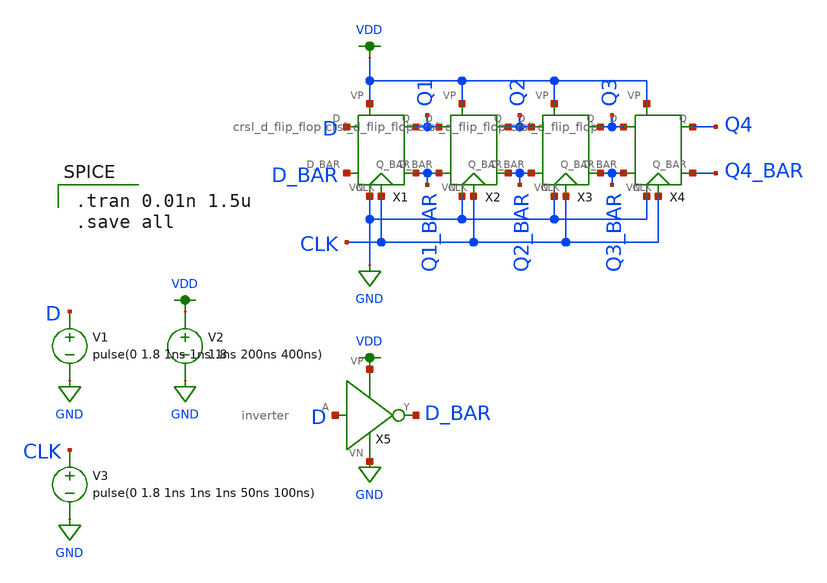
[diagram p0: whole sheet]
** sch_path: mp2/schematics/crsl_d_flip_flop_tran.sch
**.subckt crsl_d_flip_flop_tran
V1 D GND pulse(0 1.8 1ns 1ns 1ns 200ns 400ns)
X4 Q3 Q3_BAR Q4_BAR VDD Q4 CLK GND crsl_d_flip_flop
X5 D VDD GND D_BAR inverter
V2 VDD GND 1.8
V3 CLK GND pulse(0 1.8 1ns 1ns 1ns 50ns 100ns)
X1 D D_BAR Q1_BAR VDD Q1 CLK GND crsl_d_flip_flop
X2 Q1 Q1_BAR Q2_BAR VDD Q2 CLK GND crsl_d_flip_flop
X3 Q2 Q2_BAR Q3_BAR VDD Q3 CLK GND crsl_d_flip_flop
**** begin user architecture code

.option wnflag=1
.lib ~/skywater/skywater-pdk/libraries/sky130_fd_pr_ngspice/latest/models/sky130.lib.spice tt


.tran 0.01n 1.5u
.save all

**** end user architecture code
**.ends

* expanding   symbol:  /home/madvlsi/Documents/VLSI/mp2/schematics/crsl_d_flip_flop.sym # of pins=7
** sym_path: mp2/schematics/crsl_d_flip_flop.sym
** sch_path: mp2/schematics/crsl_d_flip_flop.sch
.subckt crsl_d_flip_flop D D_BAR Q_BAR VP Q CLK VN
*.ipin D
*.ipin D_BAR
*.iopin VP
*.iopin VN
*.opin Q
*.opin Q_BAR
*.ipin CLK
XM1 net1 CLK D VP sky130_fd_pr__pfet_01v8 L=0.15 W=1 nf=1 ad='int((nf+1)/2) * W/nf * 0.29' as='int((nf+2)/2) * W/nf * 0.29'
+ pd='2*int((nf+1)/2) * (W/nf + 0.29)' ps='2*int((nf+2)/2) * (W/nf + 0.29)' nrd='0.29 / W' nrs='0.29 / W'
+ sa=0 sb=0 sd=0 mult=1 m=1
XM2 net2 CLK D_BAR VP sky130_fd_pr__pfet_01v8 L=0.15 W=1 nf=1 ad='int((nf+1)/2) * W/nf * 0.29' as='int((nf+2)/2) * W/nf * 0.29'
+ pd='2*int((nf+1)/2) * (W/nf + 0.29)' ps='2*int((nf+2)/2) * (W/nf + 0.29)' nrd='0.29 / W' nrs='0.29 / W'
+ sa=0 sb=0 sd=0 mult=1 m=1
XM8 net2 net1 VP VP sky130_fd_pr__pfet_01v8 L=0.15 W=1 nf=1 ad='int((nf+1)/2) * W/nf * 0.29' as='int((nf+2)/2) * W/nf * 0.29'
+ pd='2*int((nf+1)/2) * (W/nf + 0.29)' ps='2*int((nf+2)/2) * (W/nf + 0.29)' nrd='0.29 / W' nrs='0.29 / W'
+ sa=0 sb=0 sd=0 mult=1 m=1
XM9 VP net2 net1 VP sky130_fd_pr__pfet_01v8 L=0.15 W=1 nf=1 ad='int((nf+1)/2) * W/nf * 0.29' as='int((nf+2)/2) * W/nf * 0.29'
+ pd='2*int((nf+1)/2) * (W/nf + 0.29)' ps='2*int((nf+2)/2) * (W/nf + 0.29)' nrd='0.29 / W' nrs='0.29 / W'
+ sa=0 sb=0 sd=0 mult=1 m=1
XM6 net2 net1 net3 VN sky130_fd_pr__nfet_01v8 L=0.15 W=1 nf=1 ad='int((nf+1)/2) * W/nf * 0.29' as='int((nf+2)/2) * W/nf * 0.29'
+ pd='2*int((nf+1)/2) * (W/nf + 0.29)' ps='2*int((nf+2)/2) * (W/nf + 0.29)' nrd='0.29 / W' nrs='0.29 / W'
+ sa=0 sb=0 sd=0 mult=1 m=1
XM7 net3 net2 net1 VN sky130_fd_pr__nfet_01v8 L=0.15 W=1 nf=1 ad='int((nf+1)/2) * W/nf * 0.29' as='int((nf+2)/2) * W/nf * 0.29'
+ pd='2*int((nf+1)/2) * (W/nf + 0.29)' ps='2*int((nf+2)/2) * (W/nf + 0.29)' nrd='0.29 / W' nrs='0.29 / W'
+ sa=0 sb=0 sd=0 mult=1 m=1
XM3 Q CLK net1 VN sky130_fd_pr__nfet_01v8 L=0.15 W=1 nf=1 ad='int((nf+1)/2) * W/nf * 0.29' as='int((nf+2)/2) * W/nf * 0.29'
+ pd='2*int((nf+1)/2) * (W/nf + 0.29)' ps='2*int((nf+2)/2) * (W/nf + 0.29)' nrd='0.29 / W' nrs='0.29 / W'
+ sa=0 sb=0 sd=0 mult=1 m=1
XM4 Q_BAR CLK net2 VN sky130_fd_pr__nfet_01v8 L=0.15 W=1 nf=1 ad='int((nf+1)/2) * W/nf * 0.29' as='int((nf+2)/2) * W/nf * 0.29'
+ pd='2*int((nf+1)/2) * (W/nf + 0.29)' ps='2*int((nf+2)/2) * (W/nf + 0.29)' nrd='0.29 / W' nrs='0.29 / W'
+ sa=0 sb=0 sd=0 mult=1 m=1
XM13 Q_BAR Q VN VN sky130_fd_pr__nfet_01v8 L=0.15 W=1 nf=1 ad='int((nf+1)/2) * W/nf * 0.29' as='int((nf+2)/2) * W/nf * 0.29'
+ pd='2*int((nf+1)/2) * (W/nf + 0.29)' ps='2*int((nf+2)/2) * (W/nf + 0.29)' nrd='0.29 / W' nrs='0.29 / W'
+ sa=0 sb=0 sd=0 mult=1 m=1
XM14 VN Q_BAR Q VN sky130_fd_pr__nfet_01v8 L=0.15 W=1 nf=1 ad='int((nf+1)/2) * W/nf * 0.29' as='int((nf+2)/2) * W/nf * 0.29'
+ pd='2*int((nf+1)/2) * (W/nf + 0.29)' ps='2*int((nf+2)/2) * (W/nf + 0.29)' nrd='0.29 / W' nrs='0.29 / W'
+ sa=0 sb=0 sd=0 mult=1 m=1
XM12 net4 Q_BAR Q VP sky130_fd_pr__pfet_01v8 L=0.15 W=1 nf=1 ad='int((nf+1)/2) * W/nf * 0.29' as='int((nf+2)/2) * W/nf * 0.29'
+ pd='2*int((nf+1)/2) * (W/nf + 0.29)' ps='2*int((nf+2)/2) * (W/nf + 0.29)' nrd='0.29 / W' nrs='0.29 / W'
+ sa=0 sb=0 sd=0 mult=1 m=1
XM11 Q_BAR Q net4 VP sky130_fd_pr__pfet_01v8 L=0.15 W=1 nf=1 ad='int((nf+1)/2) * W/nf * 0.29' as='int((nf+2)/2) * W/nf * 0.29'
+ pd='2*int((nf+1)/2) * (W/nf + 0.29)' ps='2*int((nf+2)/2) * (W/nf + 0.29)' nrd='0.29 / W' nrs='0.29 / W'
+ sa=0 sb=0 sd=0 mult=1 m=1
XM5 net3 CLK VN VN sky130_fd_pr__nfet_01v8 L=0.15 W=4 nf=1 ad='int((nf+1)/2) * W/nf * 0.29' as='int((nf+2)/2) * W/nf * 0.29'
+ pd='2*int((nf+1)/2) * (W/nf + 0.29)' ps='2*int((nf+2)/2) * (W/nf + 0.29)' nrd='0.29 / W' nrs='0.29 / W'
+ sa=0 sb=0 sd=0 mult=1 m=1
XM10 net4 CLK VP VP sky130_fd_pr__pfet_01v8 L=0.15 W=1 nf=1 ad='int((nf+1)/2) * W/nf * 0.29' as='int((nf+2)/2) * W/nf * 0.29'
+ pd='2*int((nf+1)/2) * (W/nf + 0.29)' ps='2*int((nf+2)/2) * (W/nf + 0.29)' nrd='0.29 / W' nrs='0.29 / W'
+ sa=0 sb=0 sd=0 mult=1 m=1
.ends


* expanding   symbol:  /home/madvlsi/Documents/VLSI/mp2/schematics/inverter.sym # of pins=4
** sym_path: mp2/schematics/inverter.sym
** sch_path: mp2/schematics/inverter.sch
.subckt inverter A VP VN Y
*.ipin A
*.iopin VP
*.iopin VN
*.opin Y
XM2 Y A VP VP sky130_fd_pr__pfet_01v8 L=0.15 W=1 nf=1 ad='int((nf+1)/2) * W/nf * 0.29' as='int((nf+2)/2) * W/nf * 0.29'
+ pd='2*int((nf+1)/2) * (W/nf + 0.29)' ps='2*int((nf+2)/2) * (W/nf + 0.29)' nrd='0.29 / W' nrs='0.29 / W'
+ sa=0 sb=0 sd=0 mult=1 m=1
XM1 Y A VN VN sky130_fd_pr__nfet_01v8 L=0.15 W=1 nf=1 ad='int((nf+1)/2) * W/nf * 0.29' as='int((nf+2)/2) * W/nf * 0.29'
+ pd='2*int((nf+1)/2) * (W/nf + 0.29)' ps='2*int((nf+2)/2) * (W/nf + 0.29)' nrd='0.29 / W' nrs='0.29 / W'
+ sa=0 sb=0 sd=0 mult=1 m=1
.ends

.GLOBAL GND
.GLOBAL VDD
.end
